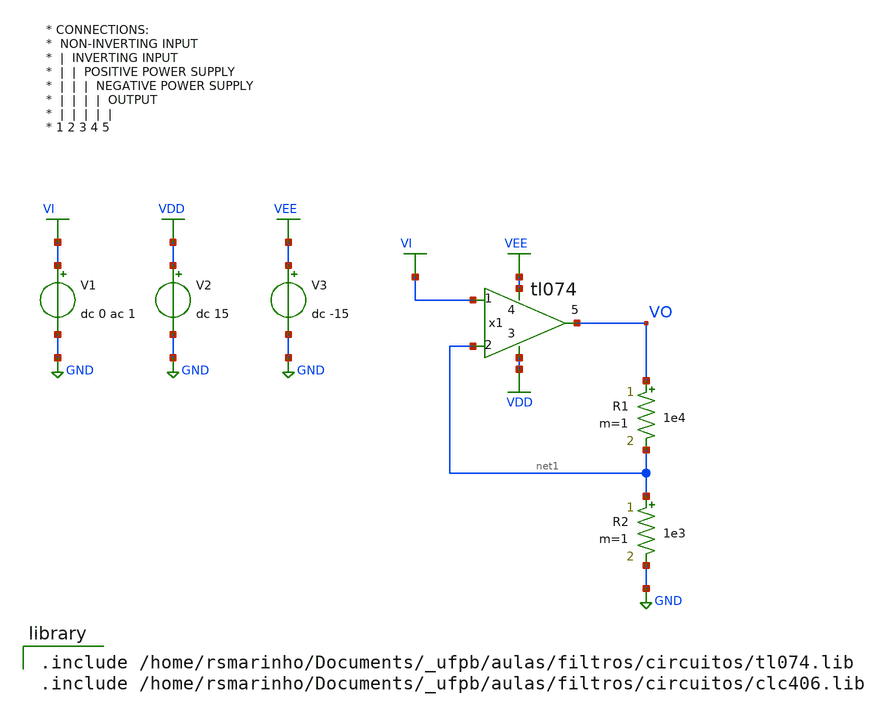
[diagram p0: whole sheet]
** sch_path: circuitos/exemplo09.sch
**.subckt exemplo09
V1 VI GND dc 0 ac 1
R1 VO net1 1e4 m=1
R2 net1 GND 1e3 m=1
V2 VDD GND dc 15
V3 VEE GND dc -15
x1 VI net1 VDD VEE VO tl074
**** begin user architecture code

.include /home/rsmarinho/Documents/_ufpb/aulas/filtros/circuitos/tl074.lib
.include /home/rsmarinho/Documents/_ufpb/aulas/filtros/circuitos/clc406.lib


.control

ac dec 1e2 1e2 1e9
plot xlog db(v(vo)/v(vi))

.endc
.end

**** end user architecture code
**.ends
.GLOBAL GND
.GLOBAL VDD
.GLOBAL VI
.GLOBAL VEE
.end
